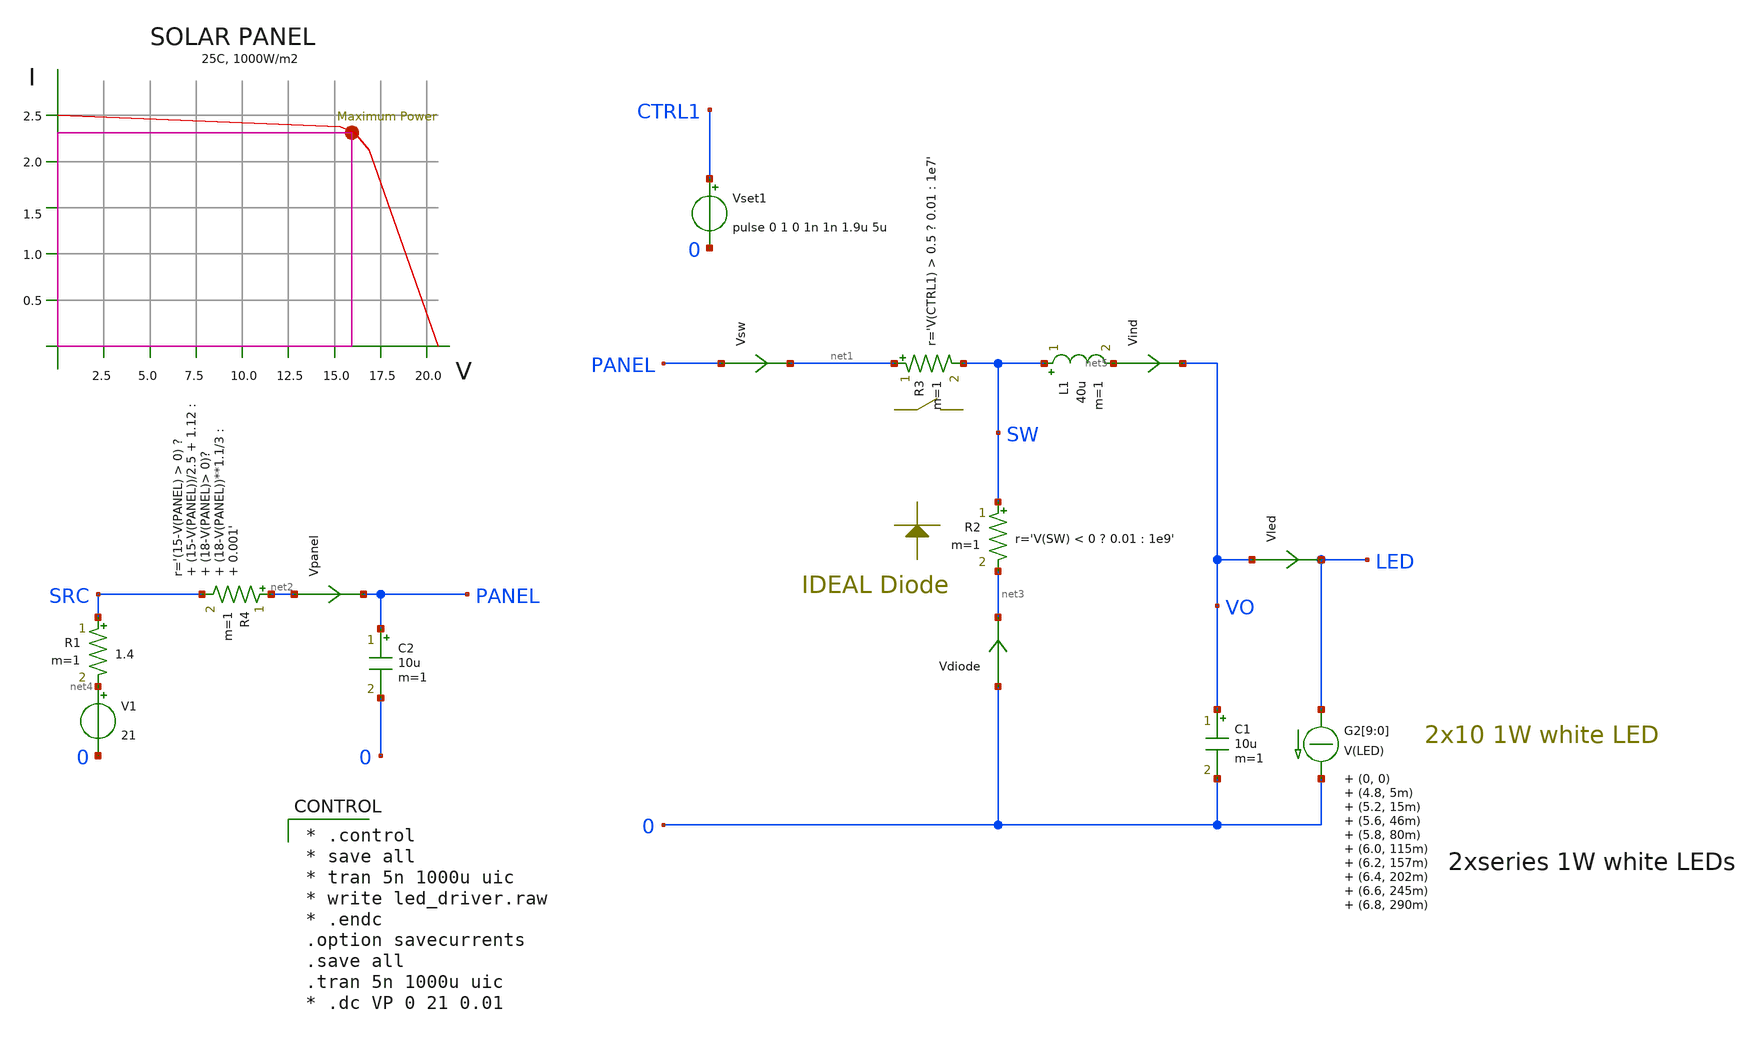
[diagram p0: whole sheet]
** sch_path: xschem_library/ngspice/solar_panel.sch
**.subckt solar_panel
V1 net4 0 21
R1 SRC net4 1.4 m=1
Vled VO LED 0
.save i(vled)
L1 SW net5 40u m=1
C1 VO 0 10u m=1
Vpanel net2 PANEL 0
.save i(vpanel)
R2 SW net3 r='V(SW) < 0 ? 0.01 : 1e9' m=1
Vset1 CTRL1 0 pulse 0 1 0 1n 1n 1.9u 5u
R3 net1 SW r='V(CTRL1) > 0.5 ? 0.01 : 1e7' m=1
R4 net2 SRC r='(15-V(PANEL) > 0) ? (15-V(PANEL))/2.5 + 1.12 : (18-V(PANEL)> 0)? (18-V(PANEL))**1.1/3 : 0.001'
+ m=1
Vind net5 VO 0
.save i(vind)
C2 PANEL 0 10u m=1
G2[9] LED 0 TABLE { V(LED) } = (0, 0) (4.8, 5m) (5.2, 15m) (5.6, 46m) (5.8, 80m) (6.0, 115m) (6.2, 157m)
+ (6.4, 202m) (6.6, 245m) (6.8, 290m) (7.0, 337m) (7.2, 395m) (7.4, 470m) (8.0, 750m)
G2[8] LED 0 TABLE { V(LED) } = (0, 0) (4.8, 5m) (5.2, 15m) (5.6, 46m) (5.8, 80m) (6.0, 115m) (6.2, 157m)
+ (6.4, 202m) (6.6, 245m) (6.8, 290m) (7.0, 337m) (7.2, 395m) (7.4, 470m) (8.0, 750m)
G2[7] LED 0 TABLE { V(LED) } = (0, 0) (4.8, 5m) (5.2, 15m) (5.6, 46m) (5.8, 80m) (6.0, 115m) (6.2, 157m)
+ (6.4, 202m) (6.6, 245m) (6.8, 290m) (7.0, 337m) (7.2, 395m) (7.4, 470m) (8.0, 750m)
G2[6] LED 0 TABLE { V(LED) } = (0, 0) (4.8, 5m) (5.2, 15m) (5.6, 46m) (5.8, 80m) (6.0, 115m) (6.2, 157m)
+ (6.4, 202m) (6.6, 245m) (6.8, 290m) (7.0, 337m) (7.2, 395m) (7.4, 470m) (8.0, 750m)
G2[5] LED 0 TABLE { V(LED) } = (0, 0) (4.8, 5m) (5.2, 15m) (5.6, 46m) (5.8, 80m) (6.0, 115m) (6.2, 157m)
+ (6.4, 202m) (6.6, 245m) (6.8, 290m) (7.0, 337m) (7.2, 395m) (7.4, 470m) (8.0, 750m)
G2[4] LED 0 TABLE { V(LED) } = (0, 0) (4.8, 5m) (5.2, 15m) (5.6, 46m) (5.8, 80m) (6.0, 115m) (6.2, 157m)
+ (6.4, 202m) (6.6, 245m) (6.8, 290m) (7.0, 337m) (7.2, 395m) (7.4, 470m) (8.0, 750m)
G2[3] LED 0 TABLE { V(LED) } = (0, 0) (4.8, 5m) (5.2, 15m) (5.6, 46m) (5.8, 80m) (6.0, 115m) (6.2, 157m)
+ (6.4, 202m) (6.6, 245m) (6.8, 290m) (7.0, 337m) (7.2, 395m) (7.4, 470m) (8.0, 750m)
G2[2] LED 0 TABLE { V(LED) } = (0, 0) (4.8, 5m) (5.2, 15m) (5.6, 46m) (5.8, 80m) (6.0, 115m) (6.2, 157m)
+ (6.4, 202m) (6.6, 245m) (6.8, 290m) (7.0, 337m) (7.2, 395m) (7.4, 470m) (8.0, 750m)
G2[1] LED 0 TABLE { V(LED) } = (0, 0) (4.8, 5m) (5.2, 15m) (5.6, 46m) (5.8, 80m) (6.0, 115m) (6.2, 157m)
+ (6.4, 202m) (6.6, 245m) (6.8, 290m) (7.0, 337m) (7.2, 395m) (7.4, 470m) (8.0, 750m)
G2[0] LED 0 TABLE { V(LED) } = (0, 0) (4.8, 5m) (5.2, 15m) (5.6, 46m) (5.8, 80m) (6.0, 115m) (6.2, 157m)
+ (6.4, 202m) (6.6, 245m) (6.8, 290m) (7.0, 337m) (7.2, 395m) (7.4, 470m) (8.0, 750m)
Vsw PANEL net1 0
.save i(vsw)
Vdiode 0 net3 0
.save i(vdiode)
**** begin user architecture code

* .control
* save all
* tran 5n 1000u uic
* write led_driver.raw
* .endc
.option savecurrents
.save all
.tran 5n 1000u uic
* .dc VP 0 21 0.01



.MODEL DIODE D(IS=1.139e-08 RS=0.99 CJO=9.3e-12 VJ=1.6 M=0.411 BV=30 EG=0.7 )
.MODEL swmod SW(VT=0.1 VH=0.01 RON=0.01 ROFF=10000000)


**** end user architecture code
**.ends
.end
